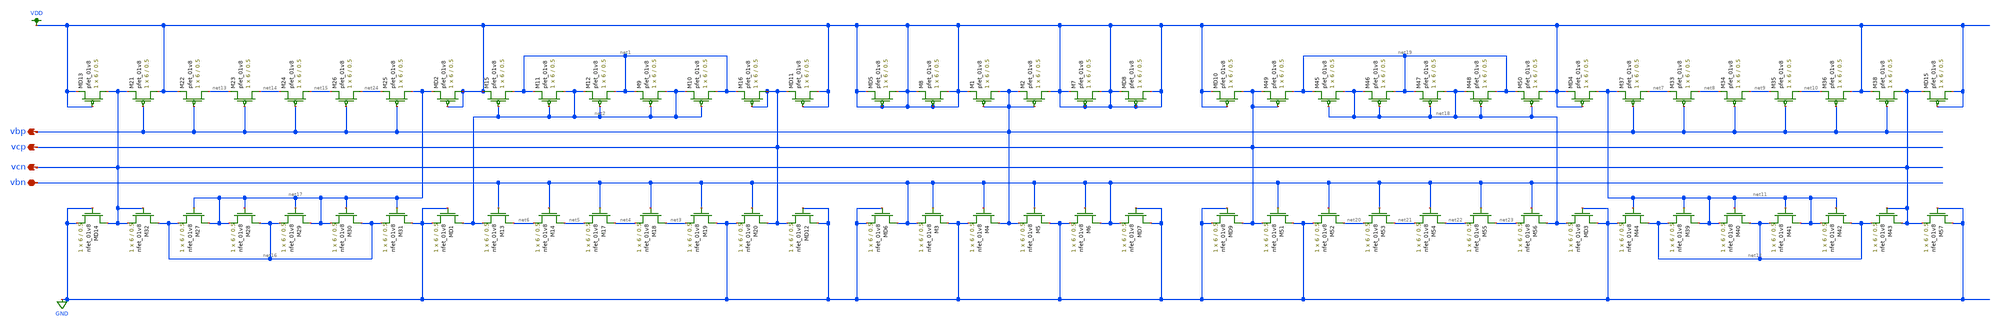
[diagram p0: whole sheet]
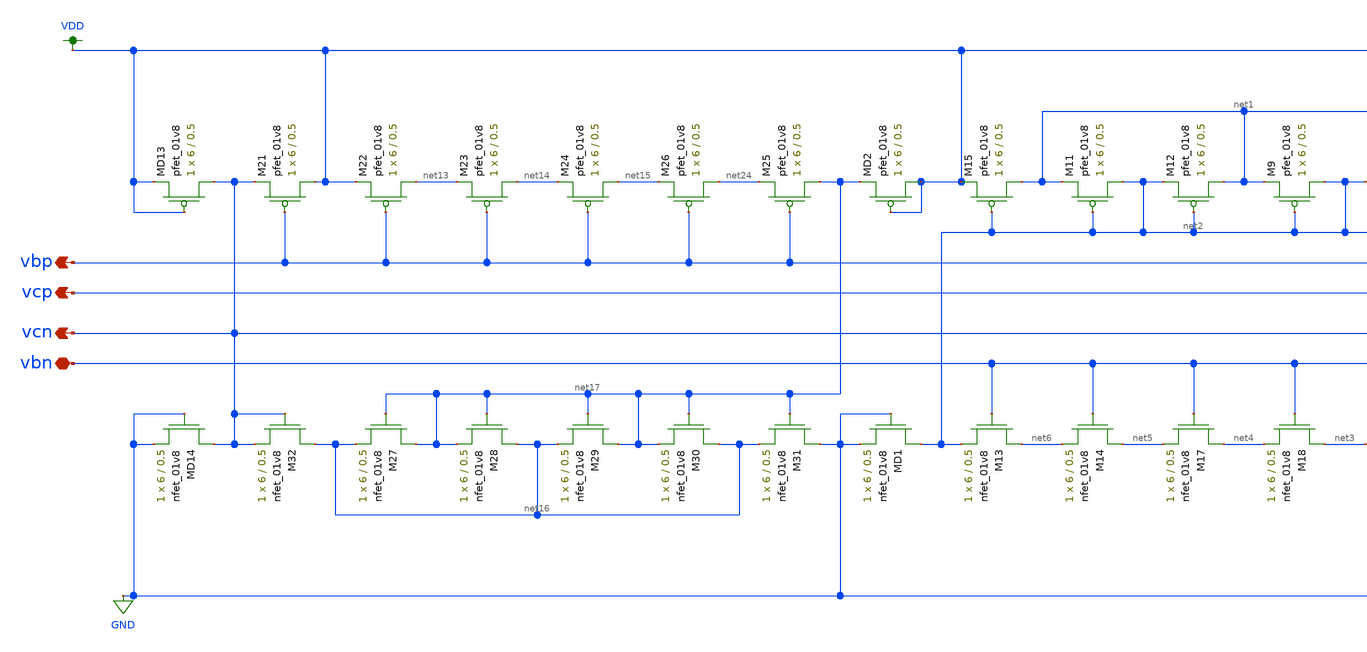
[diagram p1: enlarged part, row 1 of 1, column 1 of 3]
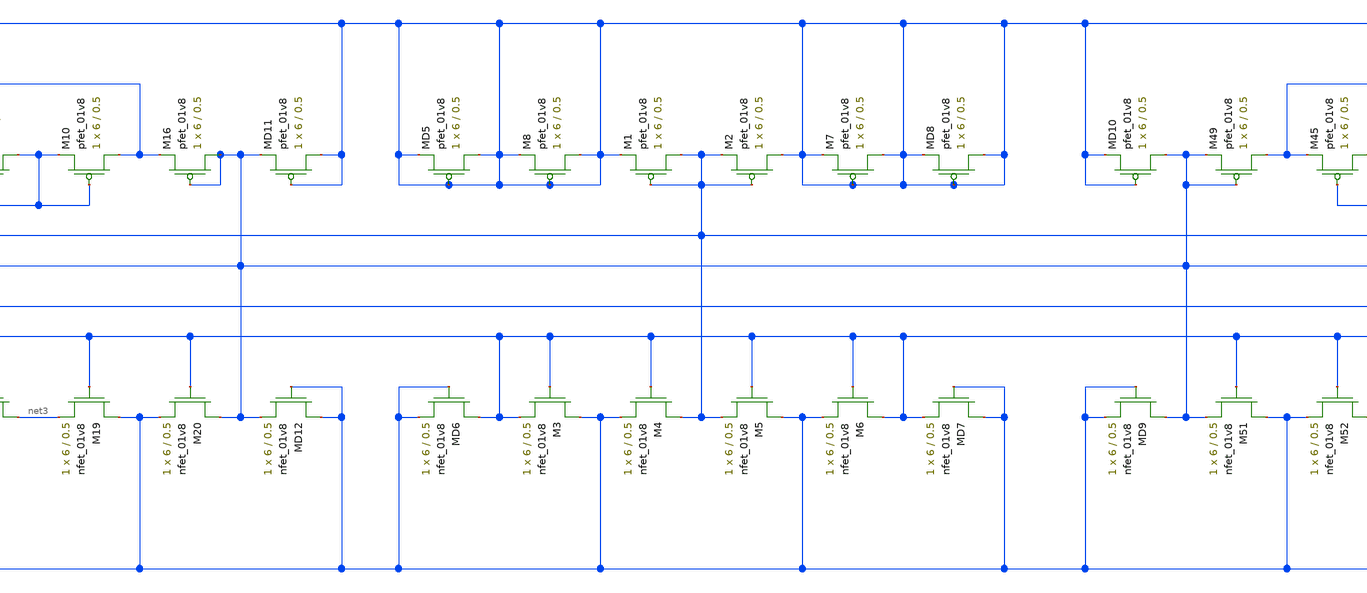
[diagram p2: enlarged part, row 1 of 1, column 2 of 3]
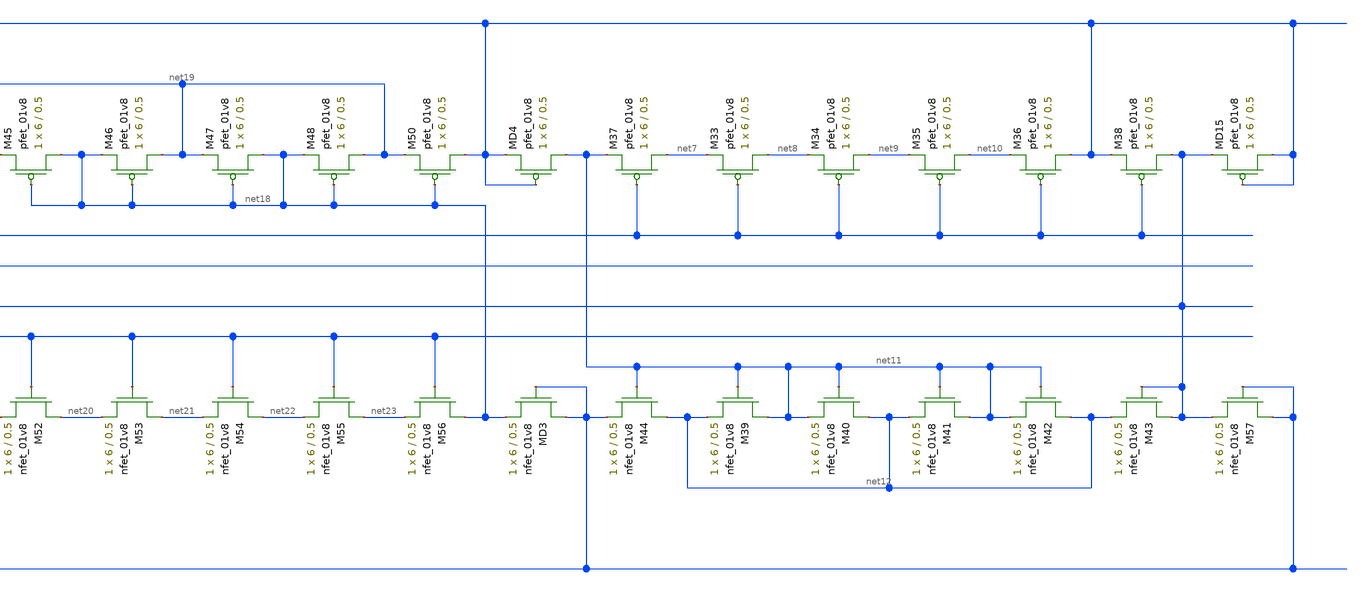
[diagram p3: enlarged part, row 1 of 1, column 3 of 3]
** sch_path: mini_proj_3/schematic/bias_generator_lvs.sch
**.subckt bias_generator_lvs vcp vcn vbp vbn
*.opin vcp
*.opin vcn
*.opin vbp
*.iopin vbn
XM3 GND vbn vbn GND sky130_fd_pr__nfet_01v8 L=0.5 W=6 nf=1 ad='int((nf+1)/2) * W/nf * 0.29' as='int((nf+2)/2) * W/nf * 0.29'
+ pd='2*int((nf+1)/2) * (W/nf + 0.29)' ps='2*int((nf+2)/2) * (W/nf + 0.29)' nrd='0.29 / W' nrs='0.29 / W'
+ sa=0 sb=0 sd=0 mult=1 m=1
XM8 VDD VDD VDD VDD sky130_fd_pr__pfet_01v8 L=0.5 W=6 nf=1 ad='int((nf+1)/2) * W/nf * 0.29' as='int((nf+2)/2) * W/nf * 0.29'
+ pd='2*int((nf+1)/2) * (W/nf + 0.29)' ps='2*int((nf+2)/2) * (W/nf + 0.29)' nrd='0.29 / W' nrs='0.29 / W'
+ sa=0 sb=0 sd=0 mult=1 m=1
XM1 vbp vbp VDD VDD sky130_fd_pr__pfet_01v8 L=0.5 W=6 nf=1 ad='int((nf+1)/2) * W/nf * 0.29' as='int((nf+2)/2) * W/nf * 0.29'
+ pd='2*int((nf+1)/2) * (W/nf + 0.29)' ps='2*int((nf+2)/2) * (W/nf + 0.29)' nrd='0.29 / W' nrs='0.29 / W'
+ sa=0 sb=0 sd=0 mult=1 m=1
XM2 VDD vbp vbp VDD sky130_fd_pr__pfet_01v8 L=0.5 W=6 nf=1 ad='int((nf+1)/2) * W/nf * 0.29' as='int((nf+2)/2) * W/nf * 0.29'
+ pd='2*int((nf+1)/2) * (W/nf + 0.29)' ps='2*int((nf+2)/2) * (W/nf + 0.29)' nrd='0.29 / W' nrs='0.29 / W'
+ sa=0 sb=0 sd=0 mult=1 m=1
XM7 VDD VDD VDD VDD sky130_fd_pr__pfet_01v8 L=0.5 W=6 nf=1 ad='int((nf+1)/2) * W/nf * 0.29' as='int((nf+2)/2) * W/nf * 0.29'
+ pd='2*int((nf+1)/2) * (W/nf + 0.29)' ps='2*int((nf+2)/2) * (W/nf + 0.29)' nrd='0.29 / W' nrs='0.29 / W'
+ sa=0 sb=0 sd=0 mult=1 m=1
XM4 vbp vbn GND GND sky130_fd_pr__nfet_01v8 L=0.5 W=6 nf=1 ad='int((nf+1)/2) * W/nf * 0.29' as='int((nf+2)/2) * W/nf * 0.29'
+ pd='2*int((nf+1)/2) * (W/nf + 0.29)' ps='2*int((nf+2)/2) * (W/nf + 0.29)' nrd='0.29 / W' nrs='0.29 / W'
+ sa=0 sb=0 sd=0 mult=1 m=1
XM5 GND vbn vbp GND sky130_fd_pr__nfet_01v8 L=0.5 W=6 nf=1 ad='int((nf+1)/2) * W/nf * 0.29' as='int((nf+2)/2) * W/nf * 0.29'
+ pd='2*int((nf+1)/2) * (W/nf + 0.29)' ps='2*int((nf+2)/2) * (W/nf + 0.29)' nrd='0.29 / W' nrs='0.29 / W'
+ sa=0 sb=0 sd=0 mult=1 m=1
XM6 vbn vbn GND GND sky130_fd_pr__nfet_01v8 L=0.5 W=6 nf=1 ad='int((nf+1)/2) * W/nf * 0.29' as='int((nf+2)/2) * W/nf * 0.29'
+ pd='2*int((nf+1)/2) * (W/nf + 0.29)' ps='2*int((nf+2)/2) * (W/nf + 0.29)' nrd='0.29 / W' nrs='0.29 / W'
+ sa=0 sb=0 sd=0 mult=1 m=1
XM11 net2 net2 net1 VDD sky130_fd_pr__pfet_01v8 L=0.5 W=6 nf=1 ad='int((nf+1)/2) * W/nf * 0.29' as='int((nf+2)/2) * W/nf * 0.29'
+ pd='2*int((nf+1)/2) * (W/nf + 0.29)' ps='2*int((nf+2)/2) * (W/nf + 0.29)' nrd='0.29 / W' nrs='0.29 / W'
+ sa=0 sb=0 sd=0 mult=1 m=1
XM12 net1 net2 net2 VDD sky130_fd_pr__pfet_01v8 L=0.5 W=6 nf=1 ad='int((nf+1)/2) * W/nf * 0.29' as='int((nf+2)/2) * W/nf * 0.29'
+ pd='2*int((nf+1)/2) * (W/nf + 0.29)' ps='2*int((nf+2)/2) * (W/nf + 0.29)' nrd='0.29 / W' nrs='0.29 / W'
+ sa=0 sb=0 sd=0 mult=1 m=1
XM9 net2 net2 net1 VDD sky130_fd_pr__pfet_01v8 L=0.5 W=6 nf=1 ad='int((nf+1)/2) * W/nf * 0.29' as='int((nf+2)/2) * W/nf * 0.29'
+ pd='2*int((nf+1)/2) * (W/nf + 0.29)' ps='2*int((nf+2)/2) * (W/nf + 0.29)' nrd='0.29 / W' nrs='0.29 / W'
+ sa=0 sb=0 sd=0 mult=1 m=1
XM10 net1 net2 net2 VDD sky130_fd_pr__pfet_01v8 L=0.5 W=6 nf=1 ad='int((nf+1)/2) * W/nf * 0.29' as='int((nf+2)/2) * W/nf * 0.29'
+ pd='2*int((nf+1)/2) * (W/nf + 0.29)' ps='2*int((nf+2)/2) * (W/nf + 0.29)' nrd='0.29 / W' nrs='0.29 / W'
+ sa=0 sb=0 sd=0 mult=1 m=1
XM15 net1 net2 VDD VDD sky130_fd_pr__pfet_01v8 L=0.5 W=6 nf=1 ad='int((nf+1)/2) * W/nf * 0.29' as='int((nf+2)/2) * W/nf * 0.29'
+ pd='2*int((nf+1)/2) * (W/nf + 0.29)' ps='2*int((nf+2)/2) * (W/nf + 0.29)' nrd='0.29 / W' nrs='0.29 / W'
+ sa=0 sb=0 sd=0 mult=1 m=1
XM16 vcp vcp net1 VDD sky130_fd_pr__pfet_01v8 L=0.5 W=6 nf=1 ad='int((nf+1)/2) * W/nf * 0.29' as='int((nf+2)/2) * W/nf * 0.29'
+ pd='2*int((nf+1)/2) * (W/nf + 0.29)' ps='2*int((nf+2)/2) * (W/nf + 0.29)' nrd='0.29 / W' nrs='0.29 / W'
+ sa=0 sb=0 sd=0 mult=1 m=1
XM13 net6 vbn net2 GND sky130_fd_pr__nfet_01v8 L=0.5 W=6 nf=1 ad='int((nf+1)/2) * W/nf * 0.29' as='int((nf+2)/2) * W/nf * 0.29'
+ pd='2*int((nf+1)/2) * (W/nf + 0.29)' ps='2*int((nf+2)/2) * (W/nf + 0.29)' nrd='0.29 / W' nrs='0.29 / W'
+ sa=0 sb=0 sd=0 mult=1 m=1
XM14 net5 vbn net6 GND sky130_fd_pr__nfet_01v8 L=0.5 W=6 nf=1 ad='int((nf+1)/2) * W/nf * 0.29' as='int((nf+2)/2) * W/nf * 0.29'
+ pd='2*int((nf+1)/2) * (W/nf + 0.29)' ps='2*int((nf+2)/2) * (W/nf + 0.29)' nrd='0.29 / W' nrs='0.29 / W'
+ sa=0 sb=0 sd=0 mult=1 m=1
XM17 net4 vbn net5 GND sky130_fd_pr__nfet_01v8 L=0.5 W=6 nf=1 ad='int((nf+1)/2) * W/nf * 0.29' as='int((nf+2)/2) * W/nf * 0.29'
+ pd='2*int((nf+1)/2) * (W/nf + 0.29)' ps='2*int((nf+2)/2) * (W/nf + 0.29)' nrd='0.29 / W' nrs='0.29 / W'
+ sa=0 sb=0 sd=0 mult=1 m=1
XM18 net3 vbn net4 GND sky130_fd_pr__nfet_01v8 L=0.5 W=6 nf=1 ad='int((nf+1)/2) * W/nf * 0.29' as='int((nf+2)/2) * W/nf * 0.29'
+ pd='2*int((nf+1)/2) * (W/nf + 0.29)' ps='2*int((nf+2)/2) * (W/nf + 0.29)' nrd='0.29 / W' nrs='0.29 / W'
+ sa=0 sb=0 sd=0 mult=1 m=1
XM19 GND vbn net3 GND sky130_fd_pr__nfet_01v8 L=0.5 W=6 nf=1 ad='int((nf+1)/2) * W/nf * 0.29' as='int((nf+2)/2) * W/nf * 0.29'
+ pd='2*int((nf+1)/2) * (W/nf + 0.29)' ps='2*int((nf+2)/2) * (W/nf + 0.29)' nrd='0.29 / W' nrs='0.29 / W'
+ sa=0 sb=0 sd=0 mult=1 m=1
XM20 vcp vbn GND GND sky130_fd_pr__nfet_01v8 L=0.5 W=6 nf=1 ad='int((nf+1)/2) * W/nf * 0.29' as='int((nf+2)/2) * W/nf * 0.29'
+ pd='2*int((nf+1)/2) * (W/nf + 0.29)' ps='2*int((nf+2)/2) * (W/nf + 0.29)' nrd='0.29 / W' nrs='0.29 / W'
+ sa=0 sb=0 sd=0 mult=1 m=1
XM33 net8 vbp net7 VDD sky130_fd_pr__pfet_01v8 L=0.5 W=6 nf=1 ad='int((nf+1)/2) * W/nf * 0.29' as='int((nf+2)/2) * W/nf * 0.29'
+ pd='2*int((nf+1)/2) * (W/nf + 0.29)' ps='2*int((nf+2)/2) * (W/nf + 0.29)' nrd='0.29 / W' nrs='0.29 / W'
+ sa=0 sb=0 sd=0 mult=1 m=1
XM34 net9 vbp net8 VDD sky130_fd_pr__pfet_01v8 L=0.5 W=6 nf=1 ad='int((nf+1)/2) * W/nf * 0.29' as='int((nf+2)/2) * W/nf * 0.29'
+ pd='2*int((nf+1)/2) * (W/nf + 0.29)' ps='2*int((nf+2)/2) * (W/nf + 0.29)' nrd='0.29 / W' nrs='0.29 / W'
+ sa=0 sb=0 sd=0 mult=1 m=1
XM35 net10 vbp net9 VDD sky130_fd_pr__pfet_01v8 L=0.5 W=6 nf=1 ad='int((nf+1)/2) * W/nf * 0.29' as='int((nf+2)/2) * W/nf * 0.29'
+ pd='2*int((nf+1)/2) * (W/nf + 0.29)' ps='2*int((nf+2)/2) * (W/nf + 0.29)' nrd='0.29 / W' nrs='0.29 / W'
+ sa=0 sb=0 sd=0 mult=1 m=1
XM36 VDD vbp net10 VDD sky130_fd_pr__pfet_01v8 L=0.5 W=6 nf=1 ad='int((nf+1)/2) * W/nf * 0.29' as='int((nf+2)/2) * W/nf * 0.29'
+ pd='2*int((nf+1)/2) * (W/nf + 0.29)' ps='2*int((nf+2)/2) * (W/nf + 0.29)' nrd='0.29 / W' nrs='0.29 / W'
+ sa=0 sb=0 sd=0 mult=1 m=1
XM37 net7 vbp net11 VDD sky130_fd_pr__pfet_01v8 L=0.5 W=6 nf=1 ad='int((nf+1)/2) * W/nf * 0.29' as='int((nf+2)/2) * W/nf * 0.29'
+ pd='2*int((nf+1)/2) * (W/nf + 0.29)' ps='2*int((nf+2)/2) * (W/nf + 0.29)' nrd='0.29 / W' nrs='0.29 / W'
+ sa=0 sb=0 sd=0 mult=1 m=1
XM38 vcn vbp VDD VDD sky130_fd_pr__pfet_01v8 L=0.5 W=6 nf=1 ad='int((nf+1)/2) * W/nf * 0.29' as='int((nf+2)/2) * W/nf * 0.29'
+ pd='2*int((nf+1)/2) * (W/nf + 0.29)' ps='2*int((nf+2)/2) * (W/nf + 0.29)' nrd='0.29 / W' nrs='0.29 / W'
+ sa=0 sb=0 sd=0 mult=1 m=1
XM39 net11 net11 net12 GND sky130_fd_pr__nfet_01v8 L=0.5 W=6 nf=1 ad='int((nf+1)/2) * W/nf * 0.29' as='int((nf+2)/2) * W/nf * 0.29'
+ pd='2*int((nf+1)/2) * (W/nf + 0.29)' ps='2*int((nf+2)/2) * (W/nf + 0.29)' nrd='0.29 / W' nrs='0.29 / W'
+ sa=0 sb=0 sd=0 mult=1 m=1
XM40 net12 net11 net11 GND sky130_fd_pr__nfet_01v8 L=0.5 W=6 nf=1 ad='int((nf+1)/2) * W/nf * 0.29' as='int((nf+2)/2) * W/nf * 0.29'
+ pd='2*int((nf+1)/2) * (W/nf + 0.29)' ps='2*int((nf+2)/2) * (W/nf + 0.29)' nrd='0.29 / W' nrs='0.29 / W'
+ sa=0 sb=0 sd=0 mult=1 m=1
XM41 net11 net11 net12 GND sky130_fd_pr__nfet_01v8 L=0.5 W=6 nf=1 ad='int((nf+1)/2) * W/nf * 0.29' as='int((nf+2)/2) * W/nf * 0.29'
+ pd='2*int((nf+1)/2) * (W/nf + 0.29)' ps='2*int((nf+2)/2) * (W/nf + 0.29)' nrd='0.29 / W' nrs='0.29 / W'
+ sa=0 sb=0 sd=0 mult=1 m=1
XM42 net12 net11 net11 GND sky130_fd_pr__nfet_01v8 L=0.5 W=6 nf=1 ad='int((nf+1)/2) * W/nf * 0.29' as='int((nf+2)/2) * W/nf * 0.29'
+ pd='2*int((nf+1)/2) * (W/nf + 0.29)' ps='2*int((nf+2)/2) * (W/nf + 0.29)' nrd='0.29 / W' nrs='0.29 / W'
+ sa=0 sb=0 sd=0 mult=1 m=1
XM43 vcn vcn net12 GND sky130_fd_pr__nfet_01v8 L=0.5 W=6 nf=1 ad='int((nf+1)/2) * W/nf * 0.29' as='int((nf+2)/2) * W/nf * 0.29'
+ pd='2*int((nf+1)/2) * (W/nf + 0.29)' ps='2*int((nf+2)/2) * (W/nf + 0.29)' nrd='0.29 / W' nrs='0.29 / W'
+ sa=0 sb=0 sd=0 mult=1 m=1
XM44 net12 net11 GND GND sky130_fd_pr__nfet_01v8 L=0.5 W=6 nf=1 ad='int((nf+1)/2) * W/nf * 0.29' as='int((nf+2)/2) * W/nf * 0.29'
+ pd='2*int((nf+1)/2) * (W/nf + 0.29)' ps='2*int((nf+2)/2) * (W/nf + 0.29)' nrd='0.29 / W' nrs='0.29 / W'
+ sa=0 sb=0 sd=0 mult=1 m=1
XM21 VDD vbp vcn VDD sky130_fd_pr__pfet_01v8 L=0.5 W=6 nf=1 ad='int((nf+1)/2) * W/nf * 0.29' as='int((nf+2)/2) * W/nf * 0.29'
+ pd='2*int((nf+1)/2) * (W/nf + 0.29)' ps='2*int((nf+2)/2) * (W/nf + 0.29)' nrd='0.29 / W' nrs='0.29 / W'
+ sa=0 sb=0 sd=0 mult=1 m=1
XM22 net13 vbp VDD VDD sky130_fd_pr__pfet_01v8 L=0.5 W=6 nf=1 ad='int((nf+1)/2) * W/nf * 0.29' as='int((nf+2)/2) * W/nf * 0.29'
+ pd='2*int((nf+1)/2) * (W/nf + 0.29)' ps='2*int((nf+2)/2) * (W/nf + 0.29)' nrd='0.29 / W' nrs='0.29 / W'
+ sa=0 sb=0 sd=0 mult=1 m=1
XM23 net14 vbp net13 VDD sky130_fd_pr__pfet_01v8 L=0.5 W=6 nf=1 ad='int((nf+1)/2) * W/nf * 0.29' as='int((nf+2)/2) * W/nf * 0.29'
+ pd='2*int((nf+1)/2) * (W/nf + 0.29)' ps='2*int((nf+2)/2) * (W/nf + 0.29)' nrd='0.29 / W' nrs='0.29 / W'
+ sa=0 sb=0 sd=0 mult=1 m=1
XM24 net15 vbp net14 VDD sky130_fd_pr__pfet_01v8 L=0.5 W=6 nf=1 ad='int((nf+1)/2) * W/nf * 0.29' as='int((nf+2)/2) * W/nf * 0.29'
+ pd='2*int((nf+1)/2) * (W/nf + 0.29)' ps='2*int((nf+2)/2) * (W/nf + 0.29)' nrd='0.29 / W' nrs='0.29 / W'
+ sa=0 sb=0 sd=0 mult=1 m=1
XM25 net17 vbp net24 VDD sky130_fd_pr__pfet_01v8 L=0.5 W=6 nf=1 ad='int((nf+1)/2) * W/nf * 0.29' as='int((nf+2)/2) * W/nf * 0.29'
+ pd='2*int((nf+1)/2) * (W/nf + 0.29)' ps='2*int((nf+2)/2) * (W/nf + 0.29)' nrd='0.29 / W' nrs='0.29 / W'
+ sa=0 sb=0 sd=0 mult=1 m=1
XM26 net24 vbp net15 VDD sky130_fd_pr__pfet_01v8 L=0.5 W=6 nf=1 ad='int((nf+1)/2) * W/nf * 0.29' as='int((nf+2)/2) * W/nf * 0.29'
+ pd='2*int((nf+1)/2) * (W/nf + 0.29)' ps='2*int((nf+2)/2) * (W/nf + 0.29)' nrd='0.29 / W' nrs='0.29 / W'
+ sa=0 sb=0 sd=0 mult=1 m=1
XM27 net17 net17 net16 GND sky130_fd_pr__nfet_01v8 L=0.5 W=6 nf=1 ad='int((nf+1)/2) * W/nf * 0.29' as='int((nf+2)/2) * W/nf * 0.29'
+ pd='2*int((nf+1)/2) * (W/nf + 0.29)' ps='2*int((nf+2)/2) * (W/nf + 0.29)' nrd='0.29 / W' nrs='0.29 / W'
+ sa=0 sb=0 sd=0 mult=1 m=1
XM28 net16 net17 net17 GND sky130_fd_pr__nfet_01v8 L=0.5 W=6 nf=1 ad='int((nf+1)/2) * W/nf * 0.29' as='int((nf+2)/2) * W/nf * 0.29'
+ pd='2*int((nf+1)/2) * (W/nf + 0.29)' ps='2*int((nf+2)/2) * (W/nf + 0.29)' nrd='0.29 / W' nrs='0.29 / W'
+ sa=0 sb=0 sd=0 mult=1 m=1
XM29 net17 net17 net16 GND sky130_fd_pr__nfet_01v8 L=0.5 W=6 nf=1 ad='int((nf+1)/2) * W/nf * 0.29' as='int((nf+2)/2) * W/nf * 0.29'
+ pd='2*int((nf+1)/2) * (W/nf + 0.29)' ps='2*int((nf+2)/2) * (W/nf + 0.29)' nrd='0.29 / W' nrs='0.29 / W'
+ sa=0 sb=0 sd=0 mult=1 m=1
XM30 net16 net17 net17 GND sky130_fd_pr__nfet_01v8 L=0.5 W=6 nf=1 ad='int((nf+1)/2) * W/nf * 0.29' as='int((nf+2)/2) * W/nf * 0.29'
+ pd='2*int((nf+1)/2) * (W/nf + 0.29)' ps='2*int((nf+2)/2) * (W/nf + 0.29)' nrd='0.29 / W' nrs='0.29 / W'
+ sa=0 sb=0 sd=0 mult=1 m=1
XM31 GND net17 net16 GND sky130_fd_pr__nfet_01v8 L=0.5 W=6 nf=1 ad='int((nf+1)/2) * W/nf * 0.29' as='int((nf+2)/2) * W/nf * 0.29'
+ pd='2*int((nf+1)/2) * (W/nf + 0.29)' ps='2*int((nf+2)/2) * (W/nf + 0.29)' nrd='0.29 / W' nrs='0.29 / W'
+ sa=0 sb=0 sd=0 mult=1 m=1
XM32 net16 vcn vcn GND sky130_fd_pr__nfet_01v8 L=0.5 W=6 nf=1 ad='int((nf+1)/2) * W/nf * 0.29' as='int((nf+2)/2) * W/nf * 0.29'
+ pd='2*int((nf+1)/2) * (W/nf + 0.29)' ps='2*int((nf+2)/2) * (W/nf + 0.29)' nrd='0.29 / W' nrs='0.29 / W'
+ sa=0 sb=0 sd=0 mult=1 m=1
XM45 net18 net18 net19 VDD sky130_fd_pr__pfet_01v8 L=0.5 W=6 nf=1 ad='int((nf+1)/2) * W/nf * 0.29' as='int((nf+2)/2) * W/nf * 0.29'
+ pd='2*int((nf+1)/2) * (W/nf + 0.29)' ps='2*int((nf+2)/2) * (W/nf + 0.29)' nrd='0.29 / W' nrs='0.29 / W'
+ sa=0 sb=0 sd=0 mult=1 m=1
XM46 net19 net18 net18 VDD sky130_fd_pr__pfet_01v8 L=0.5 W=6 nf=1 ad='int((nf+1)/2) * W/nf * 0.29' as='int((nf+2)/2) * W/nf * 0.29'
+ pd='2*int((nf+1)/2) * (W/nf + 0.29)' ps='2*int((nf+2)/2) * (W/nf + 0.29)' nrd='0.29 / W' nrs='0.29 / W'
+ sa=0 sb=0 sd=0 mult=1 m=1
XM47 net18 net18 net19 VDD sky130_fd_pr__pfet_01v8 L=0.5 W=6 nf=1 ad='int((nf+1)/2) * W/nf * 0.29' as='int((nf+2)/2) * W/nf * 0.29'
+ pd='2*int((nf+1)/2) * (W/nf + 0.29)' ps='2*int((nf+2)/2) * (W/nf + 0.29)' nrd='0.29 / W' nrs='0.29 / W'
+ sa=0 sb=0 sd=0 mult=1 m=1
XM48 net19 net18 net18 VDD sky130_fd_pr__pfet_01v8 L=0.5 W=6 nf=1 ad='int((nf+1)/2) * W/nf * 0.29' as='int((nf+2)/2) * W/nf * 0.29'
+ pd='2*int((nf+1)/2) * (W/nf + 0.29)' ps='2*int((nf+2)/2) * (W/nf + 0.29)' nrd='0.29 / W' nrs='0.29 / W'
+ sa=0 sb=0 sd=0 mult=1 m=1
XM49 net19 vcp vcp VDD sky130_fd_pr__pfet_01v8 L=0.5 W=6 nf=1 ad='int((nf+1)/2) * W/nf * 0.29' as='int((nf+2)/2) * W/nf * 0.29'
+ pd='2*int((nf+1)/2) * (W/nf + 0.29)' ps='2*int((nf+2)/2) * (W/nf + 0.29)' nrd='0.29 / W' nrs='0.29 / W'
+ sa=0 sb=0 sd=0 mult=1 m=1
XM50 VDD net18 net19 VDD sky130_fd_pr__pfet_01v8 L=0.5 W=6 nf=1 ad='int((nf+1)/2) * W/nf * 0.29' as='int((nf+2)/2) * W/nf * 0.29'
+ pd='2*int((nf+1)/2) * (W/nf + 0.29)' ps='2*int((nf+2)/2) * (W/nf + 0.29)' nrd='0.29 / W' nrs='0.29 / W'
+ sa=0 sb=0 sd=0 mult=1 m=1
XM51 GND vbn vcp GND sky130_fd_pr__nfet_01v8 L=0.5 W=6 nf=1 ad='int((nf+1)/2) * W/nf * 0.29' as='int((nf+2)/2) * W/nf * 0.29'
+ pd='2*int((nf+1)/2) * (W/nf + 0.29)' ps='2*int((nf+2)/2) * (W/nf + 0.29)' nrd='0.29 / W' nrs='0.29 / W'
+ sa=0 sb=0 sd=0 mult=1 m=1
XM52 net20 vbn GND GND sky130_fd_pr__nfet_01v8 L=0.5 W=6 nf=1 ad='int((nf+1)/2) * W/nf * 0.29' as='int((nf+2)/2) * W/nf * 0.29'
+ pd='2*int((nf+1)/2) * (W/nf + 0.29)' ps='2*int((nf+2)/2) * (W/nf + 0.29)' nrd='0.29 / W' nrs='0.29 / W'
+ sa=0 sb=0 sd=0 mult=1 m=1
XM53 net21 vbn net20 GND sky130_fd_pr__nfet_01v8 L=0.5 W=6 nf=1 ad='int((nf+1)/2) * W/nf * 0.29' as='int((nf+2)/2) * W/nf * 0.29'
+ pd='2*int((nf+1)/2) * (W/nf + 0.29)' ps='2*int((nf+2)/2) * (W/nf + 0.29)' nrd='0.29 / W' nrs='0.29 / W'
+ sa=0 sb=0 sd=0 mult=1 m=1
XM54 net22 vbn net21 GND sky130_fd_pr__nfet_01v8 L=0.5 W=6 nf=1 ad='int((nf+1)/2) * W/nf * 0.29' as='int((nf+2)/2) * W/nf * 0.29'
+ pd='2*int((nf+1)/2) * (W/nf + 0.29)' ps='2*int((nf+2)/2) * (W/nf + 0.29)' nrd='0.29 / W' nrs='0.29 / W'
+ sa=0 sb=0 sd=0 mult=1 m=1
XM55 net23 vbn net22 GND sky130_fd_pr__nfet_01v8 L=0.5 W=6 nf=1 ad='int((nf+1)/2) * W/nf * 0.29' as='int((nf+2)/2) * W/nf * 0.29'
+ pd='2*int((nf+1)/2) * (W/nf + 0.29)' ps='2*int((nf+2)/2) * (W/nf + 0.29)' nrd='0.29 / W' nrs='0.29 / W'
+ sa=0 sb=0 sd=0 mult=1 m=1
XM56 net18 vbn net23 GND sky130_fd_pr__nfet_01v8 L=0.5 W=6 nf=1 ad='int((nf+1)/2) * W/nf * 0.29' as='int((nf+2)/2) * W/nf * 0.29'
+ pd='2*int((nf+1)/2) * (W/nf + 0.29)' ps='2*int((nf+2)/2) * (W/nf + 0.29)' nrd='0.29 / W' nrs='0.29 / W'
+ sa=0 sb=0 sd=0 mult=1 m=1
XMD1 net2 GND GND GND sky130_fd_pr__nfet_01v8 L=0.5 W=6 nf=1 ad='int((nf+1)/2) * W/nf * 0.29' as='int((nf+2)/2) * W/nf * 0.29'
+ pd='2*int((nf+1)/2) * (W/nf + 0.29)' ps='2*int((nf+2)/2) * (W/nf + 0.29)' nrd='0.29 / W' nrs='0.29 / W'
+ sa=0 sb=0 sd=0 mult=1 m=1
XMD2 VDD VDD net17 VDD sky130_fd_pr__pfet_01v8 L=0.5 W=6 nf=1 ad='int((nf+1)/2) * W/nf * 0.29' as='int((nf+2)/2) * W/nf * 0.29'
+ pd='2*int((nf+1)/2) * (W/nf + 0.29)' ps='2*int((nf+2)/2) * (W/nf + 0.29)' nrd='0.29 / W' nrs='0.29 / W'
+ sa=0 sb=0 sd=0 mult=1 m=1
XMD3 GND GND net18 GND sky130_fd_pr__nfet_01v8 L=0.5 W=6 nf=1 ad='int((nf+1)/2) * W/nf * 0.29' as='int((nf+2)/2) * W/nf * 0.29'
+ pd='2*int((nf+1)/2) * (W/nf + 0.29)' ps='2*int((nf+2)/2) * (W/nf + 0.29)' nrd='0.29 / W' nrs='0.29 / W'
+ sa=0 sb=0 sd=0 mult=1 m=1
XMD4 net11 VDD VDD VDD sky130_fd_pr__pfet_01v8 L=0.5 W=6 nf=1 ad='int((nf+1)/2) * W/nf * 0.29' as='int((nf+2)/2) * W/nf * 0.29'
+ pd='2*int((nf+1)/2) * (W/nf + 0.29)' ps='2*int((nf+2)/2) * (W/nf + 0.29)' nrd='0.29 / W' nrs='0.29 / W'
+ sa=0 sb=0 sd=0 mult=1 m=1
XMD7 GND GND vbn GND sky130_fd_pr__nfet_01v8 L=0.5 W=6 nf=1 ad='int((nf+1)/2) * W/nf * 0.29' as='int((nf+2)/2) * W/nf * 0.29'
+ pd='2*int((nf+1)/2) * (W/nf + 0.29)' ps='2*int((nf+2)/2) * (W/nf + 0.29)' nrd='0.29 / W' nrs='0.29 / W'
+ sa=0 sb=0 sd=0 mult=1 m=1
XMD8 VDD VDD VDD VDD sky130_fd_pr__pfet_01v8 L=0.5 W=6 nf=1 ad='int((nf+1)/2) * W/nf * 0.29' as='int((nf+2)/2) * W/nf * 0.29'
+ pd='2*int((nf+1)/2) * (W/nf + 0.29)' ps='2*int((nf+2)/2) * (W/nf + 0.29)' nrd='0.29 / W' nrs='0.29 / W'
+ sa=0 sb=0 sd=0 mult=1 m=1
XMD9 vcp GND GND GND sky130_fd_pr__nfet_01v8 L=0.5 W=6 nf=1 ad='int((nf+1)/2) * W/nf * 0.29' as='int((nf+2)/2) * W/nf * 0.29'
+ pd='2*int((nf+1)/2) * (W/nf + 0.29)' ps='2*int((nf+2)/2) * (W/nf + 0.29)' nrd='0.29 / W' nrs='0.29 / W'
+ sa=0 sb=0 sd=0 mult=1 m=1
XMD10 vcp VDD VDD VDD sky130_fd_pr__pfet_01v8 L=0.5 W=6 nf=1 ad='int((nf+1)/2) * W/nf * 0.29' as='int((nf+2)/2) * W/nf * 0.29'
+ pd='2*int((nf+1)/2) * (W/nf + 0.29)' ps='2*int((nf+2)/2) * (W/nf + 0.29)' nrd='0.29 / W' nrs='0.29 / W'
+ sa=0 sb=0 sd=0 mult=1 m=1
XMD5 VDD VDD VDD VDD sky130_fd_pr__pfet_01v8 L=0.5 W=6 nf=1 ad='int((nf+1)/2) * W/nf * 0.29' as='int((nf+2)/2) * W/nf * 0.29'
+ pd='2*int((nf+1)/2) * (W/nf + 0.29)' ps='2*int((nf+2)/2) * (W/nf + 0.29)' nrd='0.29 / W' nrs='0.29 / W'
+ sa=0 sb=0 sd=0 mult=1 m=1
XMD6 vbn GND GND GND sky130_fd_pr__nfet_01v8 L=0.5 W=6 nf=1 ad='int((nf+1)/2) * W/nf * 0.29' as='int((nf+2)/2) * W/nf * 0.29'
+ pd='2*int((nf+1)/2) * (W/nf + 0.29)' ps='2*int((nf+2)/2) * (W/nf + 0.29)' nrd='0.29 / W' nrs='0.29 / W'
+ sa=0 sb=0 sd=0 mult=1 m=1
XMD11 VDD VDD vcp VDD sky130_fd_pr__pfet_01v8 L=0.5 W=6 nf=1 ad='int((nf+1)/2) * W/nf * 0.29' as='int((nf+2)/2) * W/nf * 0.29'
+ pd='2*int((nf+1)/2) * (W/nf + 0.29)' ps='2*int((nf+2)/2) * (W/nf + 0.29)' nrd='0.29 / W' nrs='0.29 / W'
+ sa=0 sb=0 sd=0 mult=1 m=1
XMD12 GND GND vcp GND sky130_fd_pr__nfet_01v8 L=0.5 W=6 nf=1 ad='int((nf+1)/2) * W/nf * 0.29' as='int((nf+2)/2) * W/nf * 0.29'
+ pd='2*int((nf+1)/2) * (W/nf + 0.29)' ps='2*int((nf+2)/2) * (W/nf + 0.29)' nrd='0.29 / W' nrs='0.29 / W'
+ sa=0 sb=0 sd=0 mult=1 m=1
XMD13 vcn VDD VDD VDD sky130_fd_pr__pfet_01v8 L=0.5 W=6 nf=1 ad='int((nf+1)/2) * W/nf * 0.29' as='int((nf+2)/2) * W/nf * 0.29'
+ pd='2*int((nf+1)/2) * (W/nf + 0.29)' ps='2*int((nf+2)/2) * (W/nf + 0.29)' nrd='0.29 / W' nrs='0.29 / W'
+ sa=0 sb=0 sd=0 mult=1 m=1
XMD14 vcn GND GND GND sky130_fd_pr__nfet_01v8 L=0.5 W=6 nf=1 ad='int((nf+1)/2) * W/nf * 0.29' as='int((nf+2)/2) * W/nf * 0.29'
+ pd='2*int((nf+1)/2) * (W/nf + 0.29)' ps='2*int((nf+2)/2) * (W/nf + 0.29)' nrd='0.29 / W' nrs='0.29 / W'
+ sa=0 sb=0 sd=0 mult=1 m=1
XMD15 VDD VDD vcn VDD sky130_fd_pr__pfet_01v8 L=0.5 W=6 nf=1 ad='int((nf+1)/2) * W/nf * 0.29' as='int((nf+2)/2) * W/nf * 0.29'
+ pd='2*int((nf+1)/2) * (W/nf + 0.29)' ps='2*int((nf+2)/2) * (W/nf + 0.29)' nrd='0.29 / W' nrs='0.29 / W'
+ sa=0 sb=0 sd=0 mult=1 m=1
XM57 GND GND vcn GND sky130_fd_pr__nfet_01v8 L=0.5 W=6 nf=1 ad='int((nf+1)/2) * W/nf * 0.29' as='int((nf+2)/2) * W/nf * 0.29'
+ pd='2*int((nf+1)/2) * (W/nf + 0.29)' ps='2*int((nf+2)/2) * (W/nf + 0.29)' nrd='0.29 / W' nrs='0.29 / W'
+ sa=0 sb=0 sd=0 mult=1 m=1
**.ends
.GLOBAL VDD
.GLOBAL GND
.end
